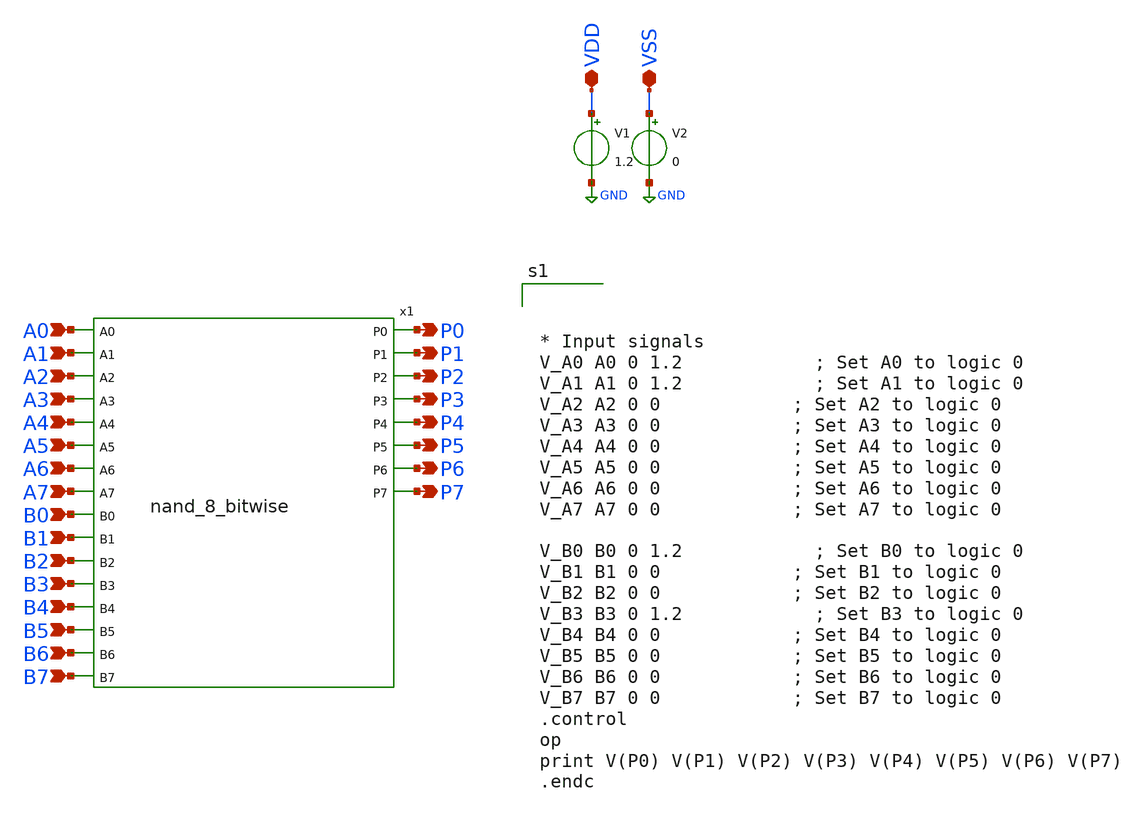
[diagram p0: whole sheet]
** sch_path: design/xschem/NAND/Nand8Tb.sch
**.subckt Nand8Tb VDD VSS A0 A1 B1 A2 B2 A3 B3 A4 B4 A5 B5 A6 B6 A7 B7 B0 P6 P7 P3 P4 P5 P0 P1 P2
*.iopin VDD
*.iopin VSS
*.ipin A0
*.ipin A1
*.ipin B1
*.ipin A2
*.ipin B2
*.ipin A3
*.ipin B3
*.ipin A4
*.ipin B4
*.ipin A5
*.ipin B5
*.ipin A6
*.ipin B6
*.ipin A7
*.ipin B7
*.ipin B0
*.opin P6
*.opin P7
*.opin P3
*.opin P4
*.opin P5
*.opin P0
*.opin P1
*.opin P2
V1 VDD GND 1.2
V2 VSS GND 0
x1 A0 A1 A2 A3 A4 A5 A6 A7 B0 B1 B2 B3 B4 B5 B6 B7 P0 P1 P2 P3 P4 P5 P6 P7 nand_8_bitwise
**** begin user architecture code

** opencircuitdesign pdks install
.lib $::SKYWATER_MODELS/sky130.lib.spice tt_mm





* Input signals
V_A0 A0 0 1.2            ; Set A0 to logic 0
V_A1 A1 0 1.2            ; Set A1 to logic 0
V_A2 A2 0 0            ; Set A2 to logic 0
V_A3 A3 0 0            ; Set A3 to logic 0
V_A4 A4 0 0            ; Set A4 to logic 0
V_A5 A5 0 0            ; Set A5 to logic 0
V_A6 A6 0 0            ; Set A6 to logic 0
V_A7 A7 0 0            ; Set A7 to logic 0

V_B0 B0 0 1.2            ; Set B0 to logic 0
V_B1 B1 0 0            ; Set B1 to logic 0
V_B2 B2 0 0            ; Set B2 to logic 0
V_B3 B3 0 1.2            ; Set B3 to logic 0
V_B4 B4 0 0            ; Set B4 to logic 0
V_B5 B5 0 0            ; Set B5 to logic 0
V_B6 B6 0 0            ; Set B6 to logic 0
V_B7 B7 0 0            ; Set B7 to logic 0
.control
op
print V(P0) V(P1) V(P2) V(P3) V(P4) V(P5) V(P6) V(P7)
.endc


**** end user architecture code
**.ends

* expanding   symbol:  NAND/nand_8_bitwise.sym # of pins=24
** sym_path: design/xschem/NAND/nand_8_bitwise.sym
** sch_path: design/xschem/NAND/nand_8_bitwise.sch
.subckt nand_8_bitwise A0 A1 A2 A3 A4 A5 A6 A7 B0 B1 B2 B3 B4 B5 B6 B7 P0 P1 P2 P3 P4 P5 P6 P7
*.ipin B7
*.ipin B5
*.ipin B6
*.ipin B4
*.ipin B3
*.ipin B2
*.ipin B1
*.ipin B0
*.opin P7
*.opin P6
*.opin P5
*.opin P4
*.opin P3
*.opin P2
*.opin P1
*.opin P0
*.ipin A7
*.ipin A5
*.ipin A6
*.ipin A4
*.ipin A3
*.ipin A2
*.ipin A1
*.ipin A0
x1 B7 A7 VSS VDD P7 nand2
x2 B6 A6 VSS VDD P6 nand2
x3 B5 A5 VSS VDD P5 nand2
x4 B4 A4 VSS VDD P4 nand2
x5 B3 A3 VSS VDD P3 nand2
x6 B2 A2 VSS VDD P2 nand2
x7 B1 A1 VSS VDD P1 nand2
x8 B0 A0 VSS VDD P0 nand2
.ends


* expanding   symbol:  NAND/nand2.sym # of pins=3
** sym_path: design/xschem/NAND/nand2.sym
** sch_path: design/xschem/NAND/nand2.sch
.subckt nand2 A B VSS VDD Y
*.ipin A
*.opin Y
*.ipin B
XM1 Y A VDD VDD sky130_fd_pr__pfet_01v8 L=0.15 W=3.2 nf=1 ad='int((nf+1)/2) * W/nf * 0.29' as='int((nf+2)/2) * W/nf * 0.29'
+ pd='2*int((nf+1)/2) * (W/nf + 0.29)' ps='2*int((nf+2)/2) * (W/nf + 0.29)' nrd='0.29 / W' nrs='0.29 / W'
+ sa=0 sb=0 sd=0 mult=1 m=1
XM2 Y A net1 net1 sky130_fd_pr__nfet_01v8 L=0.15 W=2 nf=1 ad='int((nf+1)/2) * W/nf * 0.29' as='int((nf+2)/2) * W/nf * 0.29'
+ pd='2*int((nf+1)/2) * (W/nf + 0.29)' ps='2*int((nf+2)/2) * (W/nf + 0.29)' nrd='0.29 / W' nrs='0.29 / W'
+ sa=0 sb=0 sd=0 mult=1 m=1
XM3 net1 B VSS VSS sky130_fd_pr__nfet_01v8 L=0.15 W=2 nf=1 ad='int((nf+1)/2) * W/nf * 0.29' as='int((nf+2)/2) * W/nf * 0.29'
+ pd='2*int((nf+1)/2) * (W/nf + 0.29)' ps='2*int((nf+2)/2) * (W/nf + 0.29)' nrd='0.29 / W' nrs='0.29 / W'
+ sa=0 sb=0 sd=0 mult=1 m=1
XM4 Y B VDD VDD sky130_fd_pr__pfet_01v8 L=0.15 W=3.2 nf=1 ad='int((nf+1)/2) * W/nf * 0.29' as='int((nf+2)/2) * W/nf * 0.29'
+ pd='2*int((nf+1)/2) * (W/nf + 0.29)' ps='2*int((nf+2)/2) * (W/nf + 0.29)' nrd='0.29 / W' nrs='0.29 / W'
+ sa=0 sb=0 sd=0 mult=1 m=1
.ends

.GLOBAL GND
.end
